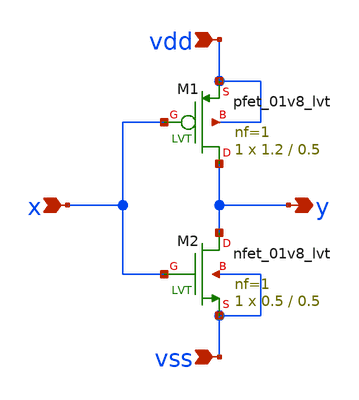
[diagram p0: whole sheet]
** sch_path: xschem/inv/inv.sch
**.subckt inv vdd vss x y
*.ipin vdd
*.ipin vss
*.ipin x
*.opin y
XM1 y x vdd vdd sky130_fd_pr__pfet_01v8_lvt L=0.5 W=1.2 nf=1 ad='int((1 + 1)/2) * 1.2 / 1 * 0.29' as='int((1 + 2)/2) * 1.2 / 1 * 0.29'
+ pd='2*int((1 + 1)/2) * (1.2 / 1 + 0.29)' ps='2*int((1 + 2)/2) * (1.2 / 1 + 0.29)' nrd='0.29 / 1.2 ' nrs='0.29 / 1.2 '
+ sa=0 sb=0 sd=0 mult=1 m=1
XM2 y x vss vss sky130_fd_pr__nfet_01v8_lvt L=0.5 W=0.5 nf=1 ad='int((1 + 1)/2) * 0.5 / 1 * 0.29' as='int((1 + 2)/2) * 0.5 / 1 * 0.29'
+ pd='2*int((1 + 1)/2) * (0.5 / 1 + 0.29)' ps='2*int((1 + 2)/2) * (0.5 / 1 + 0.29)' nrd='0.29 / 0.5 ' nrs='0.29 / 0.5 '
+ sa=0 sb=0 sd=0 mult=1 m=1
**.ends
.end
